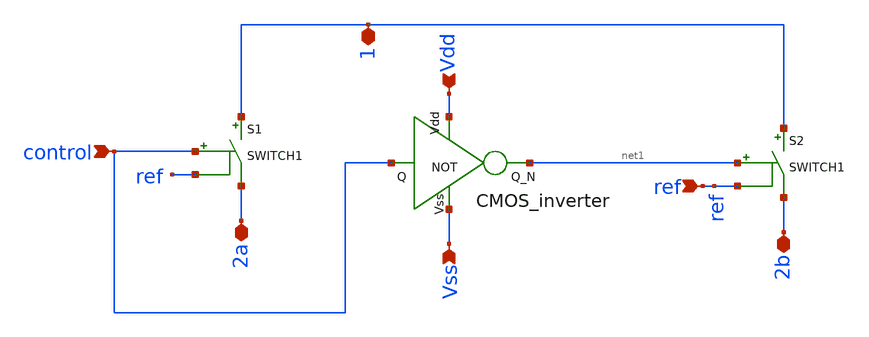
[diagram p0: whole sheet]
** sch_path: Behavioral_model/two_way_switch.sch
**.subckt two_way_switch 2b 2a ref 1 Vdd Vss control
*.iopin 2b
*.iopin 2a
*.ipin ref
*.iopin 1
*.ipin Vdd
*.ipin Vss
*.ipin control
S1 1 2a control ref SWITCH1
S2 1 2b net1 ref SWITCH1
x1 Vdd control net1 Vss CMOS_inverter
**.ends

* expanding   symbol:  CMOS_inverter.sym # of pins=4
** sym_path: Behavioral_model/CMOS_inverter.sym
** sch_path: Behavioral_model/CMOS_inverter.sch
.subckt CMOS_inverter Vdd Q Q_N Vss
*.ipin Q
*.ipin Vdd
*.ipin Vss
*.opin Q_N
XM1 Q_N Q Vss Vss sky130_fd_pr__nfet_01v8 L=0.15 W=1 nf=1 ad='int((nf+1)/2) * W/nf * 0.29' as='int((nf+2)/2) * W/nf * 0.29'
+ pd='2*int((nf+1)/2) * (W/nf + 0.29)' ps='2*int((nf+2)/2) * (W/nf + 0.29)' nrd='0.29 / W' nrs='0.29 / W'
+ sa=0 sb=0 sd=0 mult=1 m=1
XM3 Q_N Q Vdd Vdd sky130_fd_pr__pfet_01v8 L=0.15 W=1 nf=1 ad='int((nf+1)/2) * W/nf * 0.29' as='int((nf+2)/2) * W/nf * 0.29'
+ pd='2*int((nf+1)/2) * (W/nf + 0.29)' ps='2*int((nf+2)/2) * (W/nf + 0.29)' nrd='0.29 / W' nrs='0.29 / W'
+ sa=0 sb=0 sd=0 mult=1 m=1
.ends

.end
